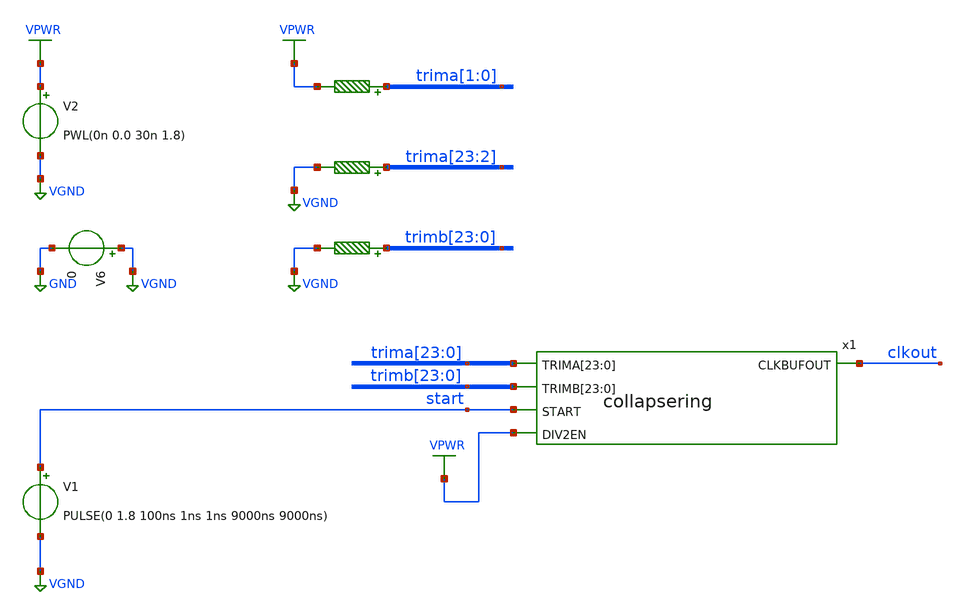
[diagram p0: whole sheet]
** sch_path: ip/randsack/sch/collapsering_tb.sch
**.subckt collapsering_tb
V1 start VGND PULSE(0 1.8 100ns 1ns 1ns 9000ns 9000ns)
V2 VPWR VGND PWL(0n 0.0 30n 1.8)
x1 trima[23] trima[22] trima[21] trima[20] trima[19] trima[18] trima[17] trima[16] trima[15]
+ trima[14] trima[13] trima[12] trima[11] trima[10] trima[9] trima[8] trima[7] trima[6] trima[5] trima[4]
+ trima[3] trima[2] trima[1] trima[0] trimb[23] trimb[22] trimb[21] trimb[20] trimb[19] trimb[18] trimb[17]
+ trimb[16] trimb[15] trimb[14] trimb[13] trimb[12] trimb[11] trimb[10] trimb[9] trimb[8] trimb[7] trimb[6]
+ trimb[5] trimb[4] trimb[3] trimb[2] trimb[1] trimb[0] start clkout VPWR collapsering
V6 VGND GND 0
R1[1] trima[1] VPWR 0.01 m=1
R1[0] trima[0] VPWR 0.01 m=1
R2[23] trima[23] VGND 0.01 m=1
R2[22] trima[22] VGND 0.01 m=1
R2[21] trima[21] VGND 0.01 m=1
R2[20] trima[20] VGND 0.01 m=1
R2[19] trima[19] VGND 0.01 m=1
R2[18] trima[18] VGND 0.01 m=1
R2[17] trima[17] VGND 0.01 m=1
R2[16] trima[16] VGND 0.01 m=1
R2[15] trima[15] VGND 0.01 m=1
R2[14] trima[14] VGND 0.01 m=1
R2[13] trima[13] VGND 0.01 m=1
R2[12] trima[12] VGND 0.01 m=1
R2[11] trima[11] VGND 0.01 m=1
R2[10] trima[10] VGND 0.01 m=1
R2[9] trima[9] VGND 0.01 m=1
R2[8] trima[8] VGND 0.01 m=1
R2[7] trima[7] VGND 0.01 m=1
R2[6] trima[6] VGND 0.01 m=1
R2[5] trima[5] VGND 0.01 m=1
R2[4] trima[4] VGND 0.01 m=1
R2[3] trima[3] VGND 0.01 m=1
R2[2] trima[2] VGND 0.01 m=1
R3[23] trimb[23] VGND 0.01 m=1
R3[22] trimb[22] VGND 0.01 m=1
R3[21] trimb[21] VGND 0.01 m=1
R3[20] trimb[20] VGND 0.01 m=1
R3[19] trimb[19] VGND 0.01 m=1
R3[18] trimb[18] VGND 0.01 m=1
R3[17] trimb[17] VGND 0.01 m=1
R3[16] trimb[16] VGND 0.01 m=1
R3[15] trimb[15] VGND 0.01 m=1
R3[14] trimb[14] VGND 0.01 m=1
R3[13] trimb[13] VGND 0.01 m=1
R3[12] trimb[12] VGND 0.01 m=1
R3[11] trimb[11] VGND 0.01 m=1
R3[10] trimb[10] VGND 0.01 m=1
R3[9] trimb[9] VGND 0.01 m=1
R3[8] trimb[8] VGND 0.01 m=1
R3[7] trimb[7] VGND 0.01 m=1
R3[6] trimb[6] VGND 0.01 m=1
R3[5] trimb[5] VGND 0.01 m=1
R3[4] trimb[4] VGND 0.01 m=1
R3[3] trimb[3] VGND 0.01 m=1
R3[2] trimb[2] VGND 0.01 m=1
R3[1] trimb[1] VGND 0.01 m=1
R3[0] trimb[0] VGND 0.01 m=1
**** begin user architecture code


.lib /home/harrison/workspace/sky130/sky130A/libs.tech/ngspice/sky130.lib.spice tt
.include /home/harrison/workspace/sky130/sky130A/libs.ref/sky130_fd_sc_hd/spice/sky130_fd_sc_hd.spice

.option TEMP=27
.option RELTOL=1.0E-1

.control
save all
tran 0.1n 10u
set appendwrite
write collapsering_tb.out
.endc


**** end user architecture code
**.ends

* expanding   symbol:  /home/harrison/workspace/randsack/ip/randsack/sch/collapsering.sym # of
*+ pins=5
** sym_path: ip/randsack/sch/collapsering.sym
** sch_path: ip/randsack/sch/collapsering.sch
.subckt collapsering TRIMA[23] TRIMA[22] TRIMA[21] TRIMA[20] TRIMA[19] TRIMA[18] TRIMA[17] TRIMA[16]
+ TRIMA[15] TRIMA[14] TRIMA[13] TRIMA[12] TRIMA[11] TRIMA[10] TRIMA[9] TRIMA[8] TRIMA[7] TRIMA[6] TRIMA[5]
+ TRIMA[4] TRIMA[3] TRIMA[2] TRIMA[1] TRIMA[0] TRIMB[23] TRIMB[22] TRIMB[21] TRIMB[20] TRIMB[19] TRIMB[18]
+ TRIMB[17] TRIMB[16] TRIMB[15] TRIMB[14] TRIMB[13] TRIMB[12] TRIMB[11] TRIMB[10] TRIMB[9] TRIMB[8] TRIMB[7]
+ TRIMB[6] TRIMB[5] TRIMB[4] TRIMB[3] TRIMB[2] TRIMB[1] TRIMB[0] START CLKBUFOUT DIV2EN
*.opin CLKBUFOUT
*.ipin START
*.ipin DIV2EN
*.ipin
*+ TRIMA[23],TRIMA[22],TRIMA[21],TRIMA[20],TRIMA[19],TRIMA[18],TRIMA[17],TRIMA[16],TRIMA[15],TRIMA[14],TRIMA[13],TRIMA[12],TRIMA[11],TRIMA[10],TRIMA[9],TRIMA[8],TRIMA[7],TRIMA[6],TRIMA[5],TRIMA[4],TRIMA[3],TRIMA[2],TRIMA[1],TRIMA[0]
*.ipin
*+ TRIMB[23],TRIMB[22],TRIMB[21],TRIMB[20],TRIMB[19],TRIMB[18],TRIMB[17],TRIMB[16],TRIMB[15],TRIMB[14],TRIMB[13],TRIMB[12],TRIMB[11],TRIMB[10],TRIMB[9],TRIMB[8],TRIMB[7],TRIMB[6],TRIMB[5],TRIMB[4],TRIMB[3],TRIMB[2],TRIMB[1],TRIMB[0]
x21 outb START VGND VNB VPB VPWR net1 sky130_fd_sc_hd__nand2_4
x47 START outa VGND VNB VPB VPWR net16 sky130_fd_sc_hd__nand2_4
x34 outa div2 DIV2EN VGND VNB VPB VPWR clkmux sky130_fd_sc_hd__mux2_4
x36 outa net25 VGND VNB VPB VPWR div2 net25 sky130_fd_sc_hd__dfxbp_2
x35 clkmux VGND VNB VPB VPWR CLKBUFOUT sky130_fd_sc_hd__clkbuf_4
x1 net2 net1 TRIMA[0] TRIMA[1] triminv
x2 net3 net2 TRIMA[2] TRIMA[3] triminv
x3 net4 net3 TRIMA[4] TRIMA[5] triminv
x4 net5 net4 TRIMA[6] TRIMA[7] triminv
x5 net6 net5 TRIMA[8] TRIMA[9] triminv
x6 net7 net6 TRIMA[10] TRIMA[11] triminv
x7 net8 net7 TRIMA[12] TRIMA[13] triminv
x8 net24 net8 TRIMA[14] TRIMA[15] triminv
x9 net17 net24 TRIMA[16] TRIMA[17] triminv
x10 net18 net17 TRIMA[18] TRIMA[19] triminv
x11 net19 net18 TRIMA[20] TRIMA[21] triminv
x12 outa net19 TRIMA[22] TRIMA[23] triminv
x13 net9 net16 TRIMB[0] TRIMB[1] triminv
x14 net10 net9 TRIMB[2] TRIMB[3] triminv
x15 net11 net10 TRIMB[4] TRIMB[5] triminv
x16 net12 net11 TRIMB[6] TRIMB[7] triminv
x17 net13 net12 TRIMB[8] TRIMB[9] triminv
x18 net14 net13 TRIMB[10] TRIMB[11] triminv
x19 net15 net14 TRIMB[12] TRIMB[13] triminv
x20 net23 net15 TRIMB[14] TRIMB[15] triminv
x22 net20 net23 TRIMB[16] TRIMB[17] triminv
x23 net21 net20 TRIMB[18] TRIMB[19] triminv
x24 net22 net21 TRIMB[20] TRIMB[21] triminv
x25 outb net22 TRIMB[22] TRIMB[23] triminv
.ends


* expanding   symbol:  /home/harrison/workspace/randsack/ip/randsack/sch/triminv.sym # of pins=4
** sym_path: ip/randsack/sch/triminv.sym
** sch_path: ip/randsack/sch/triminv.sch
.subckt triminv OUT IN TRIM0 TRIM1
*.ipin IN
*.ipin OUT
*.ipin TRIM0
*.ipin TRIM1
x1 IN VGND VNB VPB VPWR ts sky130_fd_sc_hd__clkbuf_2
x2 ts TRIM1 VGND VNB VPB VPWR d1 sky130_fd_sc_hd__einvn_4
x3 d1 VGND VNB VPB VPWR d2 sky130_fd_sc_hd__clkinv_1
x4 d2 TRIM0 VGND VNB VPB VPWR OUT sky130_fd_sc_hd__einvp_2
x5 ts VGND VNB VPB VPWR d0 sky130_fd_sc_hd__clkbuf_1
x6 d0 TRIM1 VGND VNB VPB VPWR d1 sky130_fd_sc_hd__einvp_2
x7 ts TRIM0 VGND VNB VPB VPWR OUT sky130_fd_sc_hd__einvn_8
.ends

.GLOBAL VPWR
.GLOBAL VGND
.GLOBAL GND
.end
